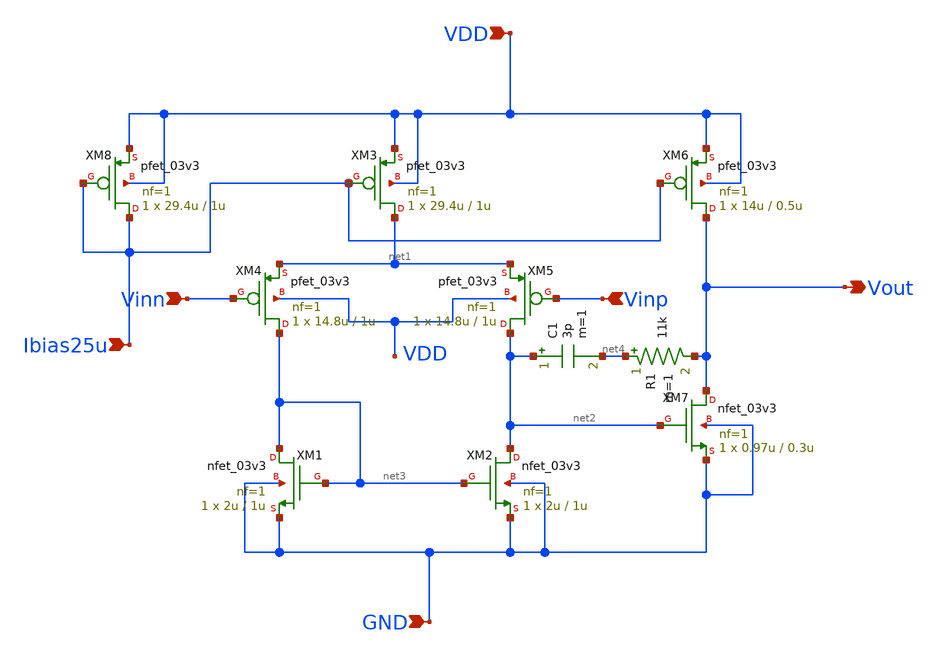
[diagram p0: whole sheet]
** sch_path: jz_tia/xschem/two_stage_miller_larger_forsym.sch
**.subckt two_stage_miller_larger_forsym Vinn Vinp Vout Ibias25u VDD GND
*.ipin Vinn
*.ipin Vinp
*.opin Vout
*.ipin Ibias25u
*.ipin VDD
*.ipin GND
XM1 net3 net3 GND GND nfet_03v3 L=1u W=2u nf=1 ad='int((nf+1)/2) * W/nf * 0.18u' as='int((nf+2)/2) * W/nf * 0.18u'
+ pd='2*int((nf+1)/2) * (W/nf + 0.18u)' ps='2*int((nf+2)/2) * (W/nf + 0.18u)' nrd='0.18u / W' nrs='0.18u / W'
+ sa=0 sb=0 sd=0 m=1
XM2 net2 net3 GND GND nfet_03v3 L=1u W=2u nf=1 ad='int((nf+1)/2) * W/nf * 0.18u' as='int((nf+2)/2) * W/nf * 0.18u'
+ pd='2*int((nf+1)/2) * (W/nf + 0.18u)' ps='2*int((nf+2)/2) * (W/nf + 0.18u)' nrd='0.18u / W' nrs='0.18u / W'
+ sa=0 sb=0 sd=0 m=1
XM3 net1 Ibias25u VDD VDD pfet_03v3 L=1u W=29.4u nf=1 ad='int((nf+1)/2) * W/nf * 0.18u' as='int((nf+2)/2) * W/nf * 0.18u'
+ pd='2*int((nf+1)/2) * (W/nf + 0.18u)' ps='2*int((nf+2)/2) * (W/nf + 0.18u)' nrd='0.18u / W' nrs='0.18u / W'
+ sa=0 sb=0 sd=0 m=1
XM4 net3 Vinn net1 VDD pfet_03v3 L=1u W=14.8u nf=1 ad='int((nf+1)/2) * W/nf * 0.18u' as='int((nf+2)/2) * W/nf * 0.18u'
+ pd='2*int((nf+1)/2) * (W/nf + 0.18u)' ps='2*int((nf+2)/2) * (W/nf + 0.18u)' nrd='0.18u / W' nrs='0.18u / W'
+ sa=0 sb=0 sd=0 m=1
XM5 net2 Vinp net1 VDD pfet_03v3 L=1u W=14.8u nf=1 ad='int((nf+1)/2) * W/nf * 0.18u' as='int((nf+2)/2) * W/nf * 0.18u'
+ pd='2*int((nf+1)/2) * (W/nf + 0.18u)' ps='2*int((nf+2)/2) * (W/nf + 0.18u)' nrd='0.18u / W' nrs='0.18u / W'
+ sa=0 sb=0 sd=0 m=1
XM6 Vout Ibias25u VDD VDD pfet_03v3 L=0.5u W=14u nf=1 ad='int((nf+1)/2) * W/nf * 0.18u' as='int((nf+2)/2) * W/nf * 0.18u'
+ pd='2*int((nf+1)/2) * (W/nf + 0.18u)' ps='2*int((nf+2)/2) * (W/nf + 0.18u)' nrd='0.18u / W' nrs='0.18u / W'
+ sa=0 sb=0 sd=0 m=1
XM7 Vout net2 GND GND nfet_03v3 L=0.3u W=0.97u nf=1 ad='int((nf+1)/2) * W/nf * 0.18u' as='int((nf+2)/2) * W/nf * 0.18u'
+ pd='2*int((nf+1)/2) * (W/nf + 0.18u)' ps='2*int((nf+2)/2) * (W/nf + 0.18u)' nrd='0.18u / W' nrs='0.18u / W'
+ sa=0 sb=0 sd=0 m=1
XM8 Ibias25u Ibias25u VDD VDD pfet_03v3 L=1u W=29.4u nf=1 ad='int((nf+1)/2) * W/nf * 0.18u' as='int((nf+2)/2) * W/nf * 0.18u'
+ pd='2*int((nf+1)/2) * (W/nf + 0.18u)' ps='2*int((nf+2)/2) * (W/nf + 0.18u)' nrd='0.18u / W' nrs='0.18u / W'
+ sa=0 sb=0 sd=0 m=1
C1 net2 net4 3p m=1
R1 net4 Vout 11k m=1
**.ends
.end
